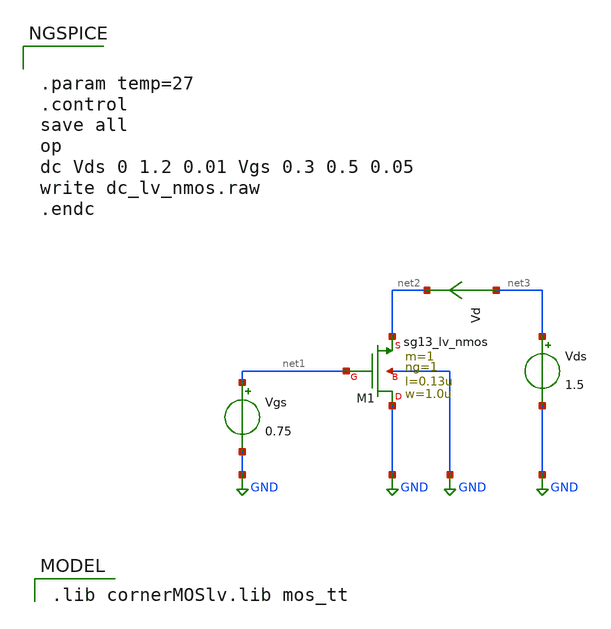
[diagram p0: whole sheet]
** sch_path: ihp-sg13g2/libs.tech/xschem/sg13g2_tests/dc_lv_nmos.sch
* Copyright 2023 IHP PDK Authors
**.subckt dc_lv_nmos
Vgs net1 GND 0.75
Vds net3 GND 1.5
Vd net3 net2 0
.save i(vd)
XM1 GND net1 net2 GND sg13_lv_nmos w=1.0u l=0.13u ng=1 m=1 mm_ok=1
**** begin user architecture code
 .lib cornerMOSlv.lib mos_tt



.param temp=27
.control
save all
op
dc Vds 0 1.2 0.01 Vgs 0.3 0.5 0.05
write dc_lv_nmos.raw
.endc


**** end user architecture code
**.ends
.GLOBAL GND
.end
